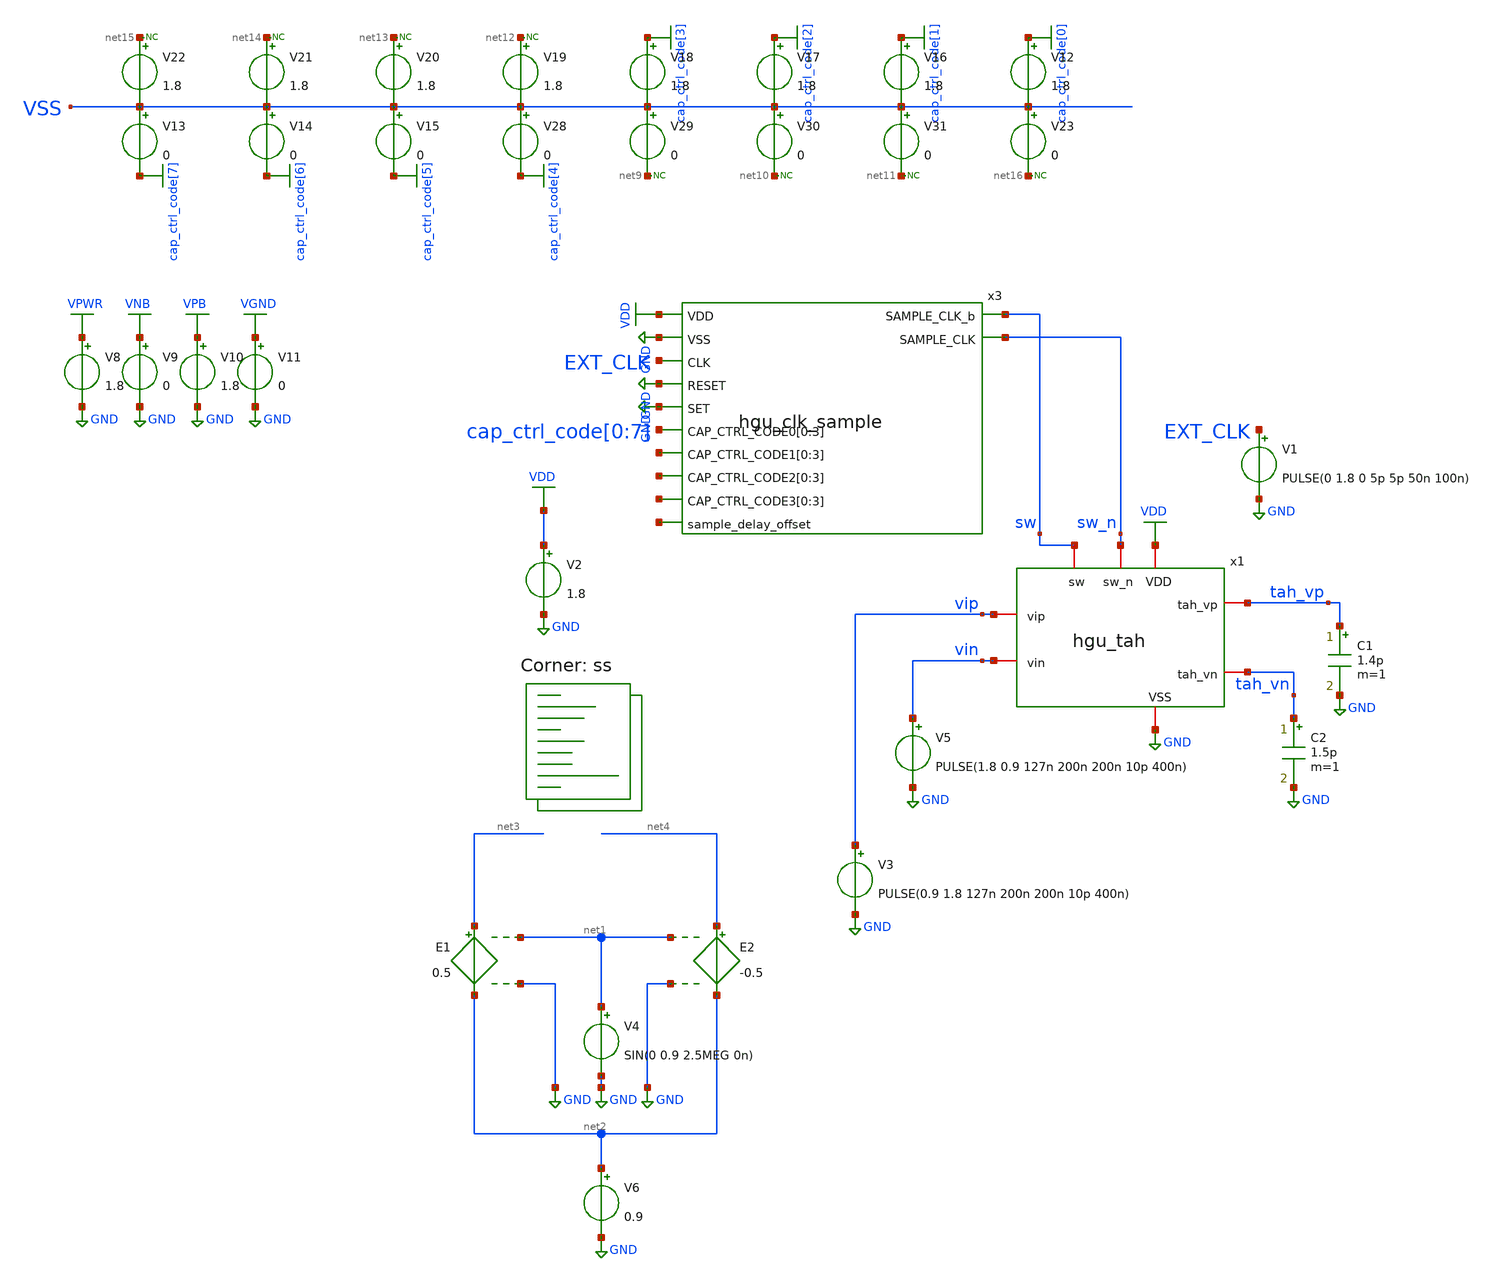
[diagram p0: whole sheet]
** sch_path: hgu/tb/tb_hgu_tah_nonideal.sch
**.subckt tb_hgu_tah_nonideal
x1 sw VDD GND sw_n tah_vp vip vin tah_vn hgu_tah
V2 VDD GND 1.8
C2 tah_vn GND 1.5p m=1
C1 tah_vp GND 1.4p m=1
V1 EXT_CLK GND PULSE(0 1.8 0 5p 5p 50n 100n)
V4 net1 GND SIN(0 0.9 2.5MEG 0n)
E1 net3 net2 net1 GND 0.5
E2 net4 net2 net1 GND -0.5
V6 net2 GND 0.9
x3 sw VDD GND EXT_CLK GND GND sw_n cap_ctrl_code[0] cap_ctrl_code[1] cap_ctrl_code[2]
+ cap_ctrl_code[3] net5[3] net5[2] net5[1] net5[0] net6[3] net6[2] net6[1] net6[0] net7[3] net7[2] net7[1] net7[0]
+ net8 hgu_clk_sample
V12 cap_ctrl_code[0] VSS 1.8
V13 VSS cap_ctrl_code[7] 0
V14 VSS cap_ctrl_code[6] 0
V15 VSS cap_ctrl_code[5] 0
V28 VSS cap_ctrl_code[4] 0
V29 VSS net9 0
V30 VSS net10 0
V31 VSS net11 0
V16 cap_ctrl_code[1] VSS 1.8
V17 cap_ctrl_code[2] VSS 1.8
V18 cap_ctrl_code[3] VSS 1.8
V19 net12 VSS 1.8
V20 net13 VSS 1.8
V21 net14 VSS 1.8
V22 net15 VSS 1.8
V23 VSS net16 0
* noconn #net15
* noconn #net14
* noconn #net13
* noconn #net12
* noconn #net9
* noconn #net10
* noconn #net11
* noconn #net16
V8 VPWR GND 1.8
V9 VNB GND 0
V10 VPB GND 1.8
V11 VGND GND 0
V3 vip GND PULSE(0.9 1.8 127n 200n 200n 10p 400n)
V5 vin GND PULSE(1.8 0.9 127n 200n 200n 10p 400n)
**** begin user architecture code


.save all
.temp = 25
.tran 100p 600n
.OPTIONS savecurrents
.include /foss/pdks/sky130A/libs.ref/sky130_fd_sc_hd/spice/sky130_fd_sc_hd.spice

.control
run
	plot v(sw)-0.9 v(sw_n)-0.9 tah_vp-tah_vn vip-vin
        let svdd = 1.8
        let max = svdd*0.8
        let min = svdd*0.2
        let mid = svdd*0.5
	let input = vip-vin
        meas tran rising_s find time when V(tah_vp-tah_vn)=min RISE=1 TD=100n
        meas tran rising_e find time when V(tah_vp-tah_vn)=max RISE=1 TD=100n
        let rising_time = rising_e-rising_s
        meas tran falling_s find time when V(tah_vp-tah_vn)=max FALL=1 TD=1000p
        meas tran falling_e find time when V(tah_vp-tah_vn)=min FALL=1 TD=1000p
        let falling_time = falling_e-falling_s
        meas tran IN find time when V(sw)=mid RISE=1 TD=350n
        meas tran OUT find time when V(tah_vp-tah_vn)=mid RISE=1 TD=350n
        let rising_delay = OUT-IN
        meas tran fIN find time when V(sw)=mid RISE=1 TD=100n
        meas tran fOUT find time when V(tah_vp-tah_vn)=mid FALL=1 TD=100n
        let falling_delay = fOUT-fIN
	meas tran holdval find input when V(sw)=mid FALL=1 TD=300n


        print holdval

*plot v(sw)+2 v(sw) tah_vp tah_vn+2
*plot v(sw) tah_vp-tah_vn vip-vin
.endc


.lib $::SKYWATER_MODELS/sky130.lib.spice ss
**** end user architecture code
**.ends
.GLOBAL GND
.GLOBAL VDD
.GLOBAL cap_ctrl_code[7]
.GLOBAL cap_ctrl_code[6]
.GLOBAL cap_ctrl_code[5]
.GLOBAL cap_ctrl_code[4]
.GLOBAL cap_ctrl_code[3]
.GLOBAL cap_ctrl_code[2]
.GLOBAL cap_ctrl_code[1]
.GLOBAL cap_ctrl_code[0]
.GLOBAL VGND
.GLOBAL VNB
.GLOBAL VPB
.GLOBAL VPWR
.end
